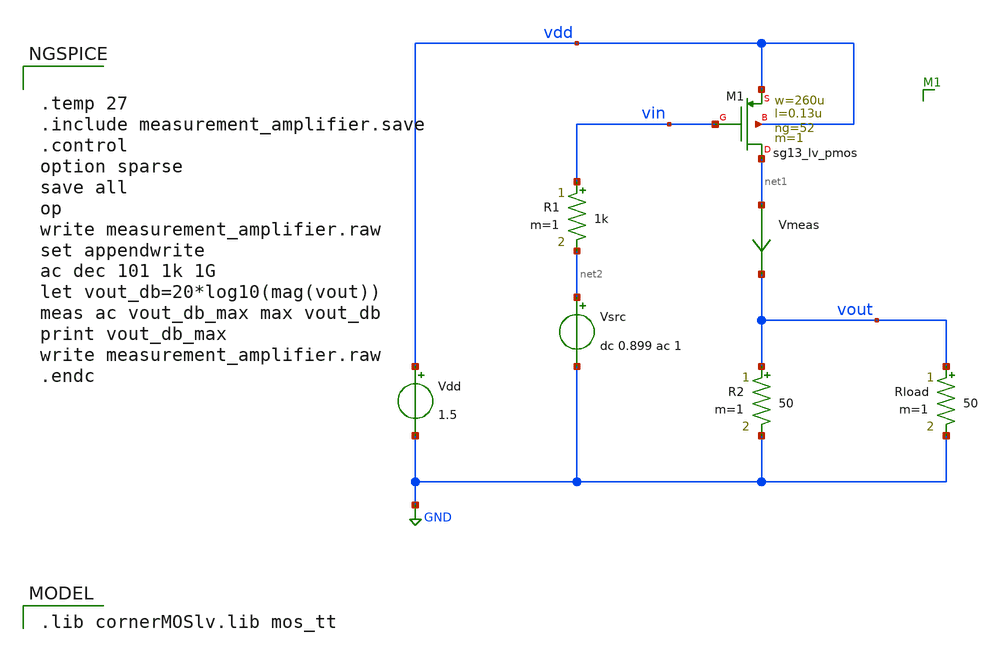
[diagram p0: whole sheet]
** sch_path: xschem/measurement_amplifier.sch
* (c) 2024-2025 Harald Pretl, Apache-2.0 license
**.subckt measurement_amplifier
Vdd vdd GND 1.5
Rload vout GND 50 m=1
R2 vout GND 50 m=1
Vmeas net1 vout 0
.save i(vmeas)
XM1 net1 vin vdd vdd sg13_lv_pmos w=260u l=0.13u ng=52 m=1 mm_ok=1
Vsrc net2 GND dc 0.899 ac 1
R1 vin net2 1k m=1
**** begin user architecture code
 .lib cornerMOSlv.lib mos_tt



.temp 27
.include measurement_amplifier.save
.control
option sparse
save all
op
write measurement_amplifier.raw
set appendwrite
ac dec 101 1k 1G
let vout_db=20*log10(mag(vout))
meas ac vout_db_max max vout_db
print vout_db_max
write measurement_amplifier.raw
.endc


**** end user architecture code
**.ends
.GLOBAL GND
.end
